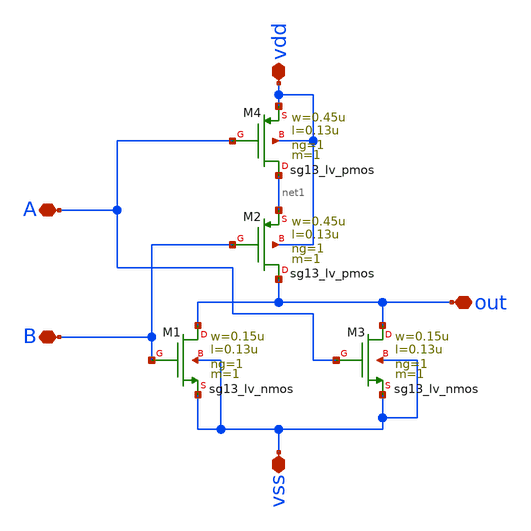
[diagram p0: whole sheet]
** sch_path: BinarytoThermo/nor_custom.sch
**.subckt nor_custom vdd vss A B out
*.iopin vdd
*.iopin vss
*.iopin A
*.iopin B
*.iopin out
XM1 out B vss vss sg13_lv_nmos w=0.15u l=0.13u ng=1 m=1 mm_ok=1
XM2 out B net1 vdd sg13_lv_pmos w=0.45u l=0.13u ng=1 m=1 mm_ok=1
XM3 out A vss vss sg13_lv_nmos w=0.15u l=0.13u ng=1 m=1 mm_ok=1
XM4 net1 A vdd vdd sg13_lv_pmos w=0.45u l=0.13u ng=1 m=1 mm_ok=1
**.ends
.end
